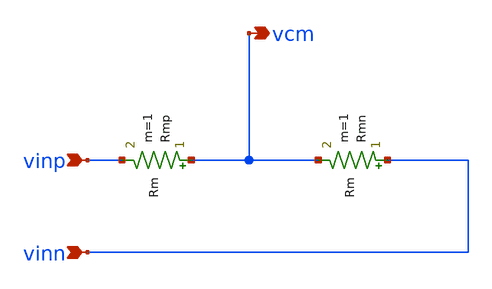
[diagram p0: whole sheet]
** sch_path: analog-db/circuits/sup_001_vcm_detector/pdk/ihp-sg13g2/schematic/vcm-detector-simple.sch
* Copyright 2026 MacAnalog Research Group
**.subckt vcm-detector-simple vinp vinn vcm
*.ipin vinp
*.ipin vinn
*.opin vcm
Rmp vcm vinp Rm m=1
Rmn vinn vcm Rm m=1
**.ends
.end
